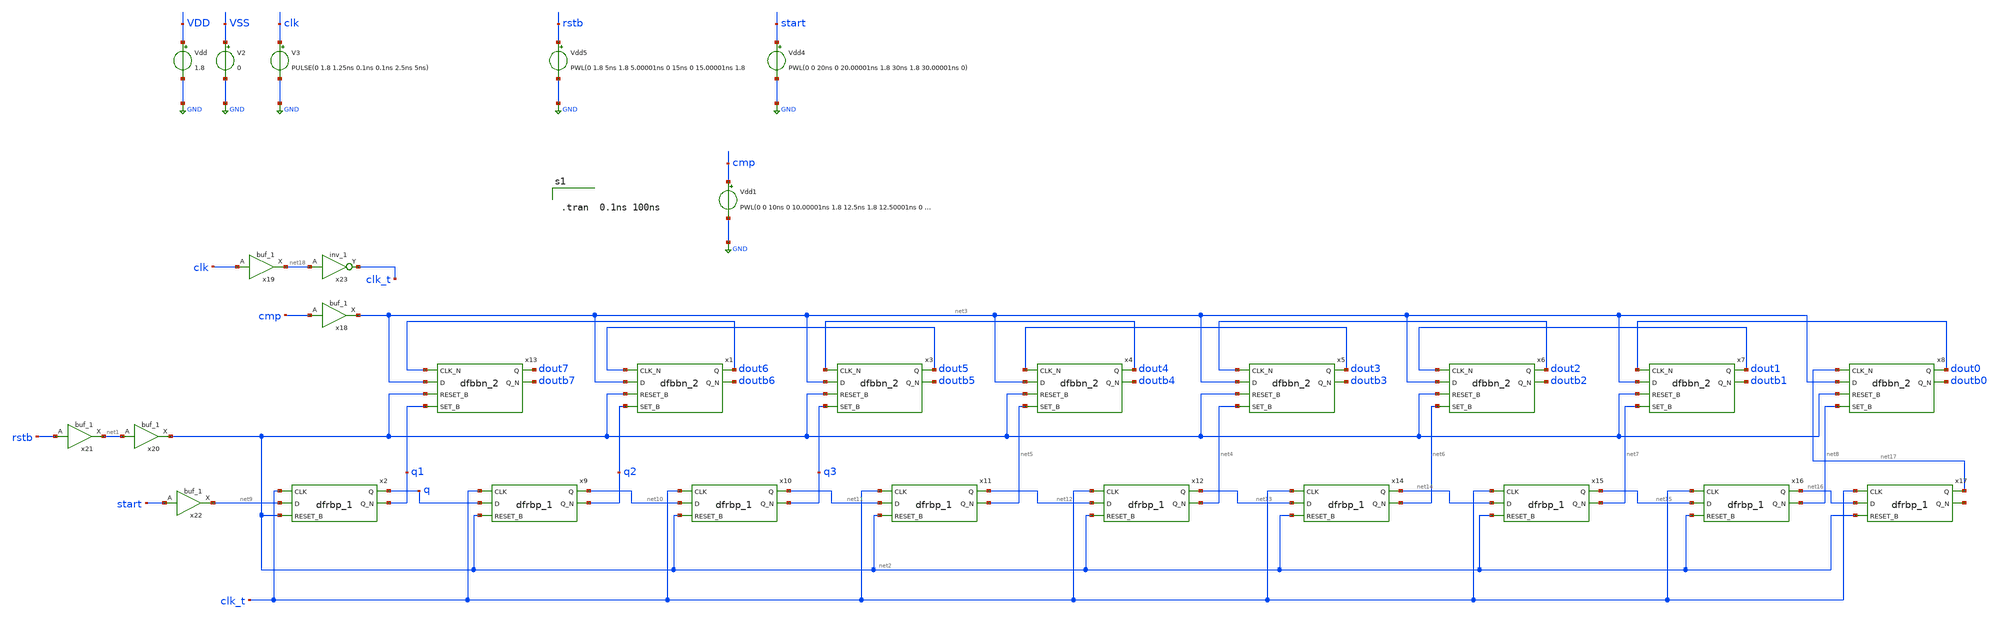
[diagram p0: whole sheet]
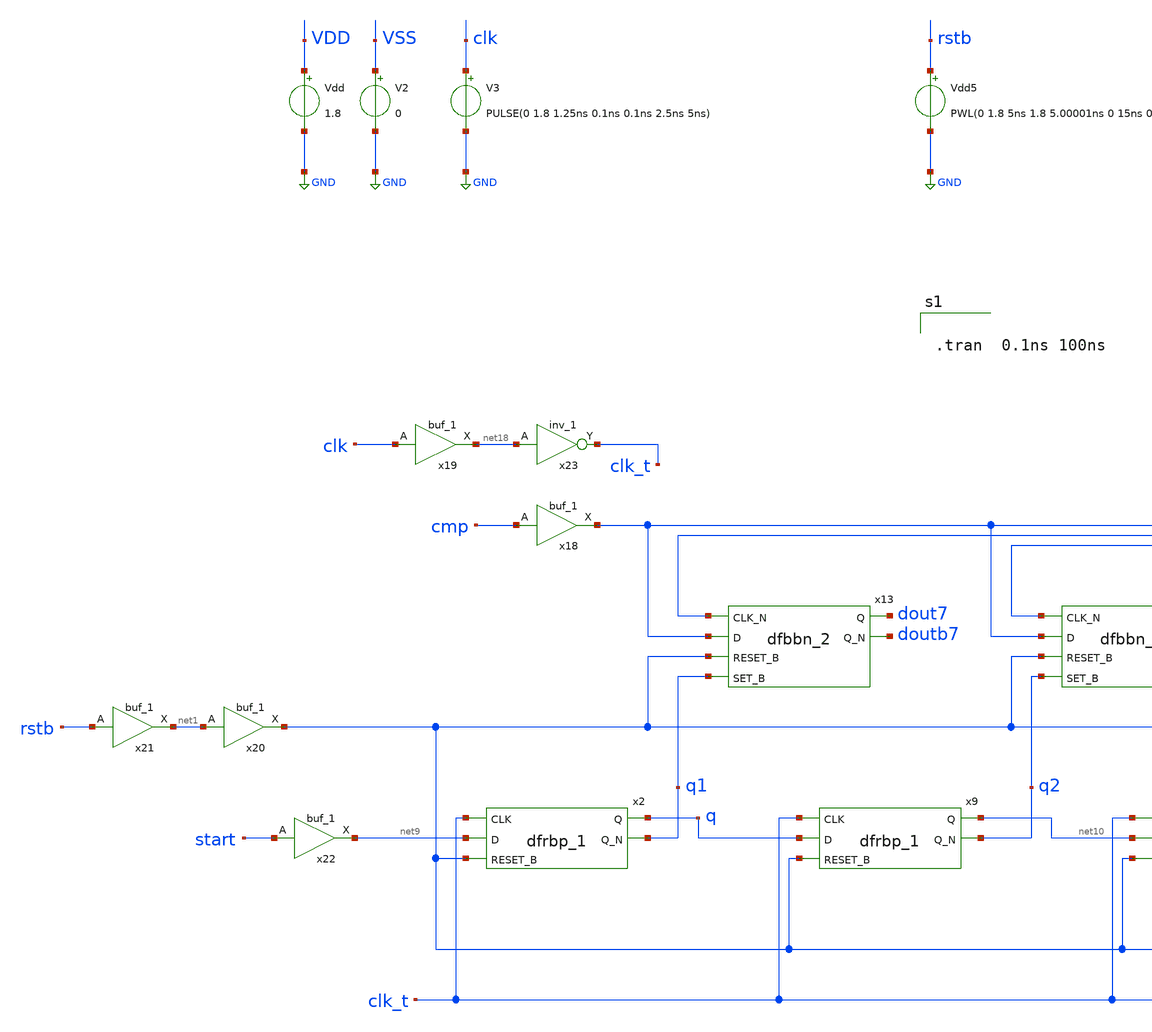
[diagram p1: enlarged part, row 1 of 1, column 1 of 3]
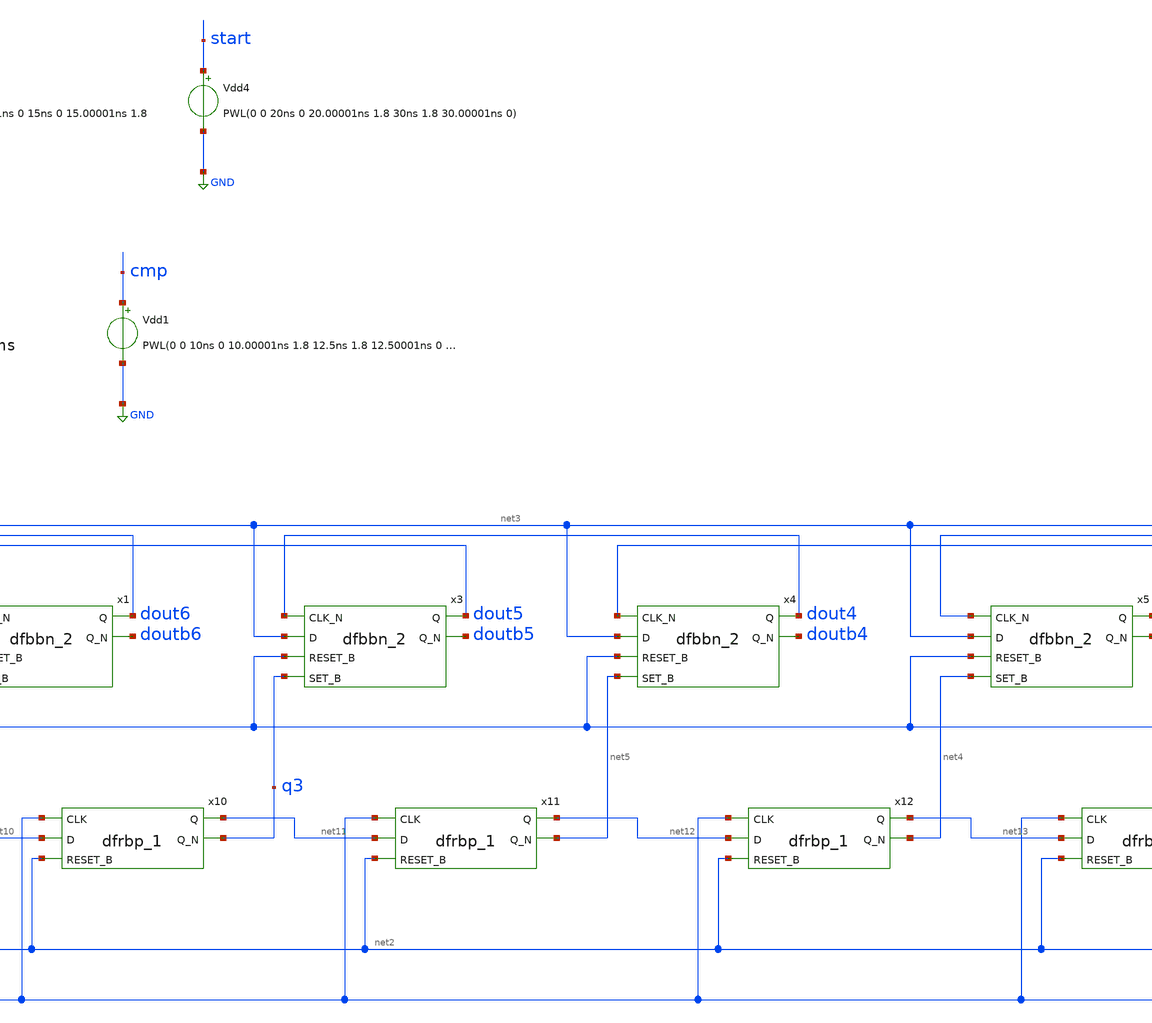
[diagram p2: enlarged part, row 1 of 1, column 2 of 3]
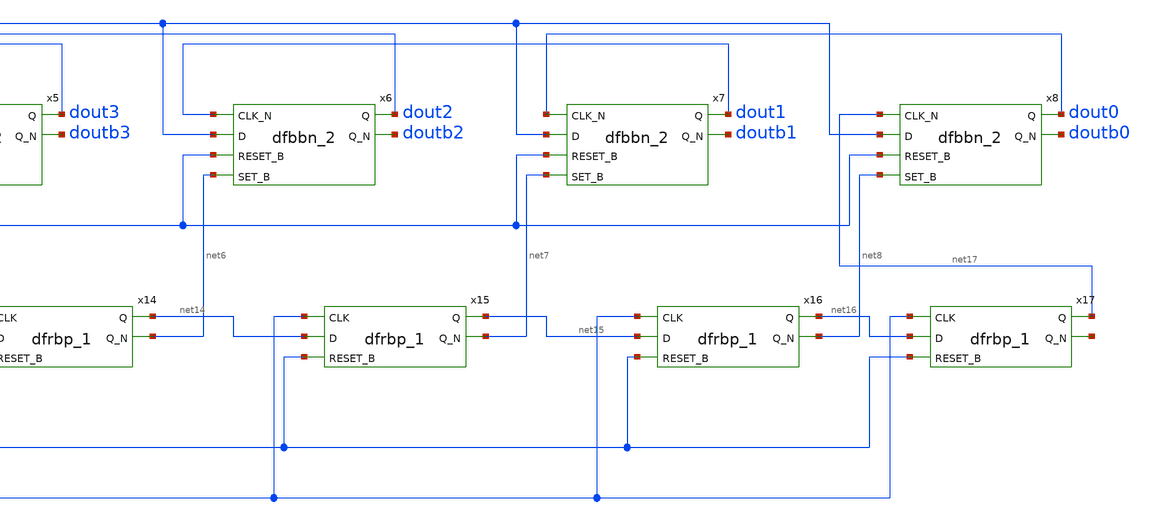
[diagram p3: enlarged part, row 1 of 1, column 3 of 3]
** sch_path: 8bitADC_SARLOGIC_dfftest.sch
**.subckt 8bitADC_SARLOGIC_dfftest
x18 cmp VSS VNB VPB VDD net3 sky130_fd_sc_hd__buf_1
x19 clk VSS VNB VPB VDD net18 sky130_fd_sc_hd__buf_1
x20 net1 VSS VNB VPB VDD net2 sky130_fd_sc_hd__buf_1
x21 rstb VSS VNB VPB VDD net1 sky130_fd_sc_hd__buf_1
x22 start VSS VNB VPB VDD net9 sky130_fd_sc_hd__buf_1
x13 dout6 net3 net2 q1 VSS VNB VPB VDD dout7 doutb7 sky130_fd_sc_hd__dfbbn_2
x1 dout5 net3 net2 q2 VSS VNB VPB VDD dout6 doutb6 sky130_fd_sc_hd__dfbbn_2
x3 dout4 net3 net2 q3 VSS VNB VPB VDD dout5 doutb5 sky130_fd_sc_hd__dfbbn_2
x4 dout3 net3 net2 net5 VSS VNB VPB VDD dout4 doutb4 sky130_fd_sc_hd__dfbbn_2
x5 dout2 net3 net2 net4 VSS VNB VPB VDD dout3 doutb3 sky130_fd_sc_hd__dfbbn_2
x6 dout1 net3 net2 net6 VSS VNB VPB VDD dout2 doutb2 sky130_fd_sc_hd__dfbbn_2
x7 dout0 net3 net2 net7 VSS VNB VPB VDD dout1 doutb1 sky130_fd_sc_hd__dfbbn_2
x8 net17 net3 net2 net8 VSS VNB VPB VDD dout0 doutb0 sky130_fd_sc_hd__dfbbn_2
Vdd VDD GND 1.8
V2 VSS GND 0
Vdd4 start GND PWL(0 0 20ns 0 20.00001ns 1.8 30ns 1.8 30.00001ns 0)
Vdd5 rstb GND PWL(0 1.8 5ns 1.8 5.00001ns 0 15ns 0 15.00001ns 1.8
x2 clk_t net9 net2 VSS VNB VPB VDD q q1 sky130_fd_sc_hd__dfrbp_1
x9 clk_t q net2 VSS VNB VPB VDD net10 q2 sky130_fd_sc_hd__dfrbp_1
x10 clk_t net10 net2 VSS VNB VPB VDD net11 q3 sky130_fd_sc_hd__dfrbp_1
x11 clk_t net11 net2 VSS VNB VPB VDD net12 net5 sky130_fd_sc_hd__dfrbp_1
x12 clk_t net12 net2 VSS VNB VPB VDD net13 net4 sky130_fd_sc_hd__dfrbp_1
x14 clk_t net13 net2 VSS VNB VPB VDD net14 net6 sky130_fd_sc_hd__dfrbp_1
x15 clk_t net14 net2 VSS VNB VPB VDD net15 net7 sky130_fd_sc_hd__dfrbp_1
x16 clk_t net15 net2 VSS VNB VPB VDD net16 net8 sky130_fd_sc_hd__dfrbp_1
x17 clk_t net16 net2 VSS VNB VPB VDD net17 net19 sky130_fd_sc_hd__dfrbp_1
V3 clk GND PULSE(0 1.8 1.25ns 0.1ns 0.1ns 2.5ns 5ns)
Vdd1 cmp GND PWL(0 0 10ns 0 10.00001ns 1.8 12.5ns 1.8 12.50001ns 0 20ns 0 20.0001ns 1.8 22.5ns 1.8
+ 22.50001ns 0 40ns 0 40.0001ns 1.8 42.5ns 1.8 42.50001ns 0)
x23 net18 VSS VNB VPB VDD clk_t sky130_fd_sc_hd__inv_1
**** begin user architecture code

** opencircuitdesign pdks install
.lib $::SKYWATER_MODELS/sky130.lib.spice tt
.include $::SKYWATER_STDCELLS/sky130_fd_sc_hd.spice




.tran  0.1ns 100ns




**** end user architecture code
**.ends
.GLOBAL GND
.end
